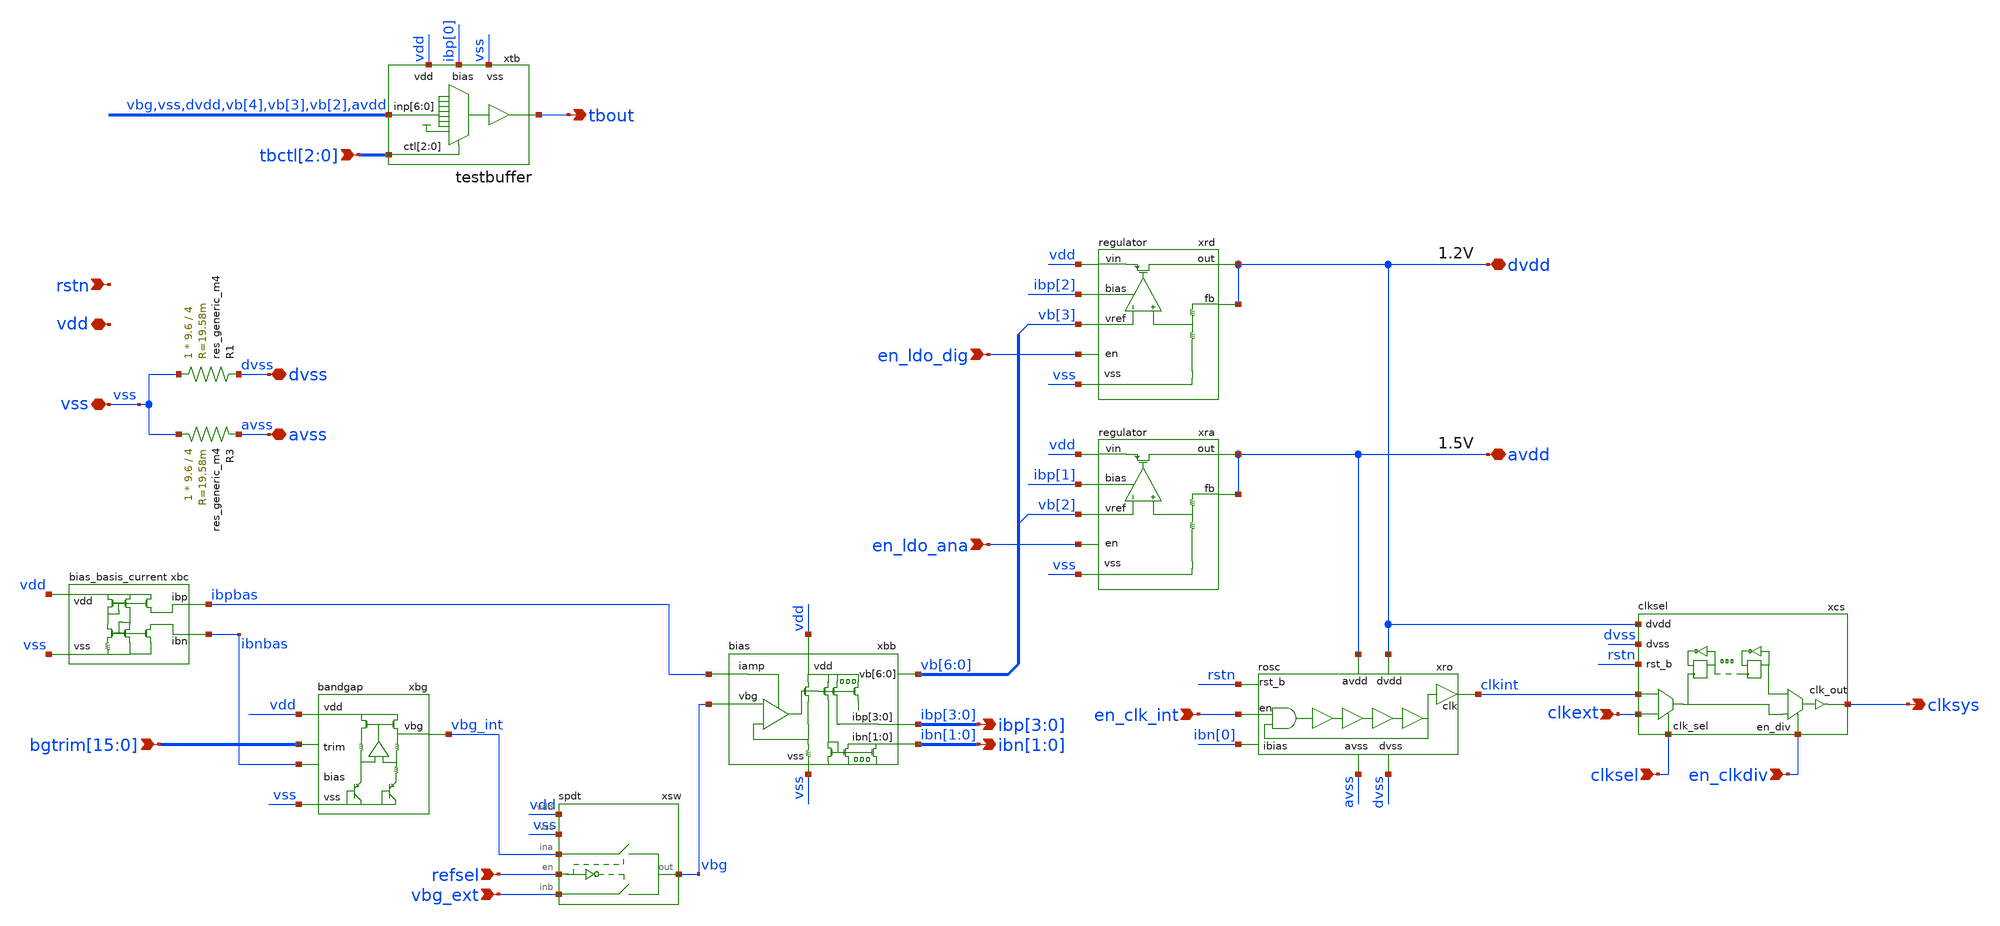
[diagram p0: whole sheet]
** sch_path: xschem/main/main.sch
**.subckt main clksel clkext en_clkdiv en_ldo_ana en_ldo_dig en_clk_int vbg_ext refsel
*+ ibp[3],ibp[2],ibp[1],ibp[0] ibn[1],ibn[0] vdd vss rstn clksys dvss avss dvdd avdd
*+ bgtrim[15],bgtrim[14],bgtrim[13],bgtrim[12],bgtrim[11],bgtrim[10],bgtrim[9],bgtrim[8],bgtrim[7],bgtrim[6],bgtrim[5],bgtrim[4],bgtrim[3],bgtrim[2],bgtrim[1],bgtrim[0] tbout tbctl[2],tbctl[1],tbctl[0]
*.ipin clksel
*.ipin clkext
*.ipin en_clkdiv
*.ipin en_ldo_ana
*.ipin en_ldo_dig
*.ipin en_clk_int
*.ipin vbg_ext
*.ipin refsel
*.opin ibp[3],ibp[2],ibp[1],ibp[0]
*.opin ibn[1],ibn[0]
*.iopin vdd
*.iopin vss
*.ipin rstn
*.opin clksys
*.iopin dvss
*.iopin avss
*.iopin dvdd
*.iopin avdd
*.ipin
*+ bgtrim[15],bgtrim[14],bgtrim[13],bgtrim[12],bgtrim[11],bgtrim[10],bgtrim[9],bgtrim[8],bgtrim[7],bgtrim[6],bgtrim[5],bgtrim[4],bgtrim[3],bgtrim[2],bgtrim[1],bgtrim[0]
*.opin tbout
*.ipin tbctl[2],tbctl[1],tbctl[0]
xbg vdd vbg_int vss ibnbas bgtrim[15] bgtrim[14] bgtrim[13] bgtrim[12] bgtrim[11] bgtrim[10]
+ bgtrim[9] bgtrim[8] bgtrim[7] bgtrim[6] bgtrim[5] bgtrim[4] bgtrim[3] bgtrim[2] bgtrim[1] bgtrim[0] bandgap
xbb ibpbas vbg ibp[3] ibp[2] ibp[1] ibp[0] ibn[1] ibn[0] vdd vss vb[6] vb[5] vb[4] vb[3] vb[2] vb[1]
+ vb[0] bias
xro avdd avss dvdd dvss rstn ibn[0] clkint en_clk_int rosc
xbc vdd vss ibpbas ibnbas bias_basis_current
xra avdd vb[2] vss vdd ibp[1] en_ldo_ana avdd regulator
xrd dvdd vb[3] vss vdd ibp[2] en_ldo_dig dvdd regulator
xcs dvdd dvss rstn clkint clksys clkext en_clkdiv clksel clksel
xsw vbg refsel vdd vbg_ext vss vbg_int spdt
xtb ibp[0] tbout vdd vss vbg vss dvdd vb[4] vb[3] vb[2] avdd tbctl[2] tbctl[1] tbctl[0] testbuffer
R3 vss avss sky130_fd_pr__res_generic_m4 W=9.6 L=4 m=1
R1 vss dvss sky130_fd_pr__res_generic_m4 W=9.6 L=4 m=1
**.ends
.end
